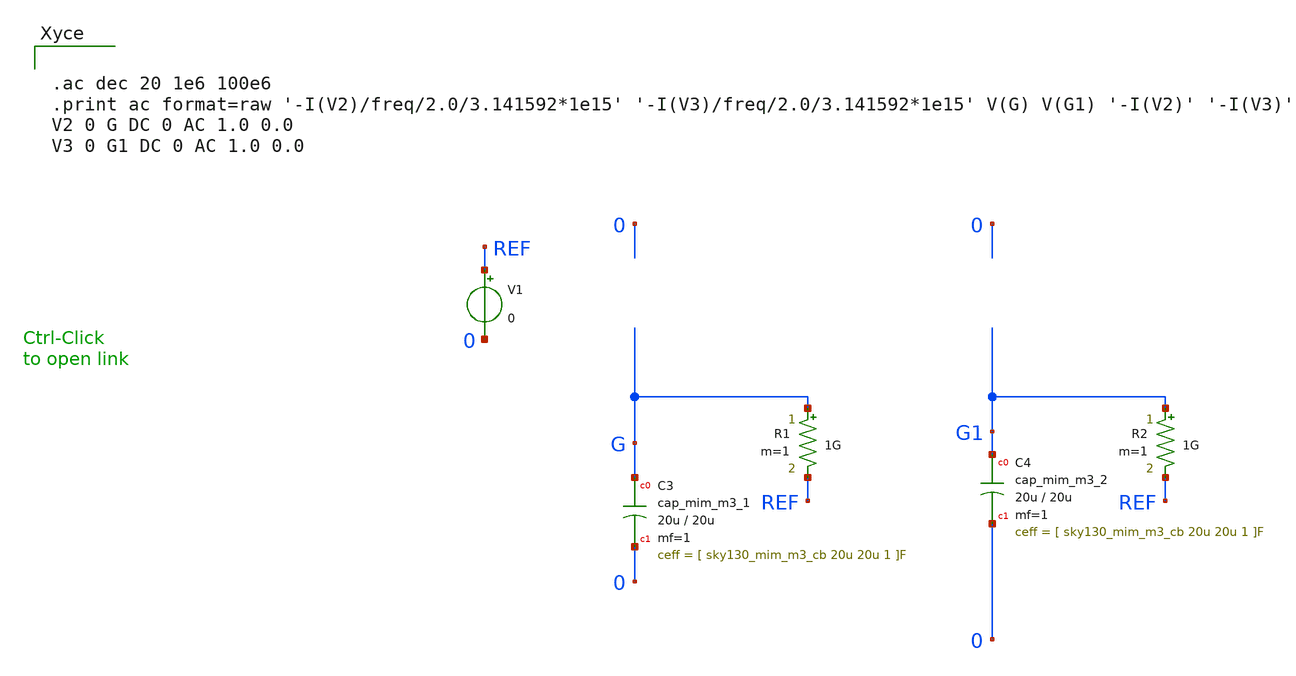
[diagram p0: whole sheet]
** sch_path: sky130_tests_X/test_mim2x.sch
* Copyright 2020 Stefan Frederik Schippers
* Licensed under the Apache License, Version 2.0 (the "License");
* you may not use this file except in compliance with the License.
* You may obtain a copy of the License at
* https://www.apache.org/licenses/LICENSE-2.0
* Unless required by applicable law or agreed to in writing, software
* distributed under the License is distributed on an "AS IS" BASIS,
* WITHOUT WARRANTIES OR CONDITIONS OF ANY KIND, either express or implied.
* See the License for the specific language governing permissions and
* limitations under the License.
**.subckt test_mim2x
R1 G REF 1G m=1
R2 G1 REF 1G m=1
V1 REF 0 0
XC4 G1 0 sky130_fd_pr__cap_mim_m3_2 w=20u l=20u mf=1
XC3 G 0 sky130_fd_pr__cap_mim_m3_1 w=20u l=20u mf=1 m=1
**** begin user architecture code


.ac dec 20 1e6 100e6
.print ac format=raw '-I(V2)/freq/2.0/3.141592*1e15' '-I(V3)/freq/2.0/3.141592*1e15' V(G) V(G1) '-I(V2)'
+ '-I(V3)'
V2 0 G DC 0 AC 1.0 0.0
V3 0 G1 DC 0 AC 1.0 0.0



**** end user architecture code
**.ends
.end
